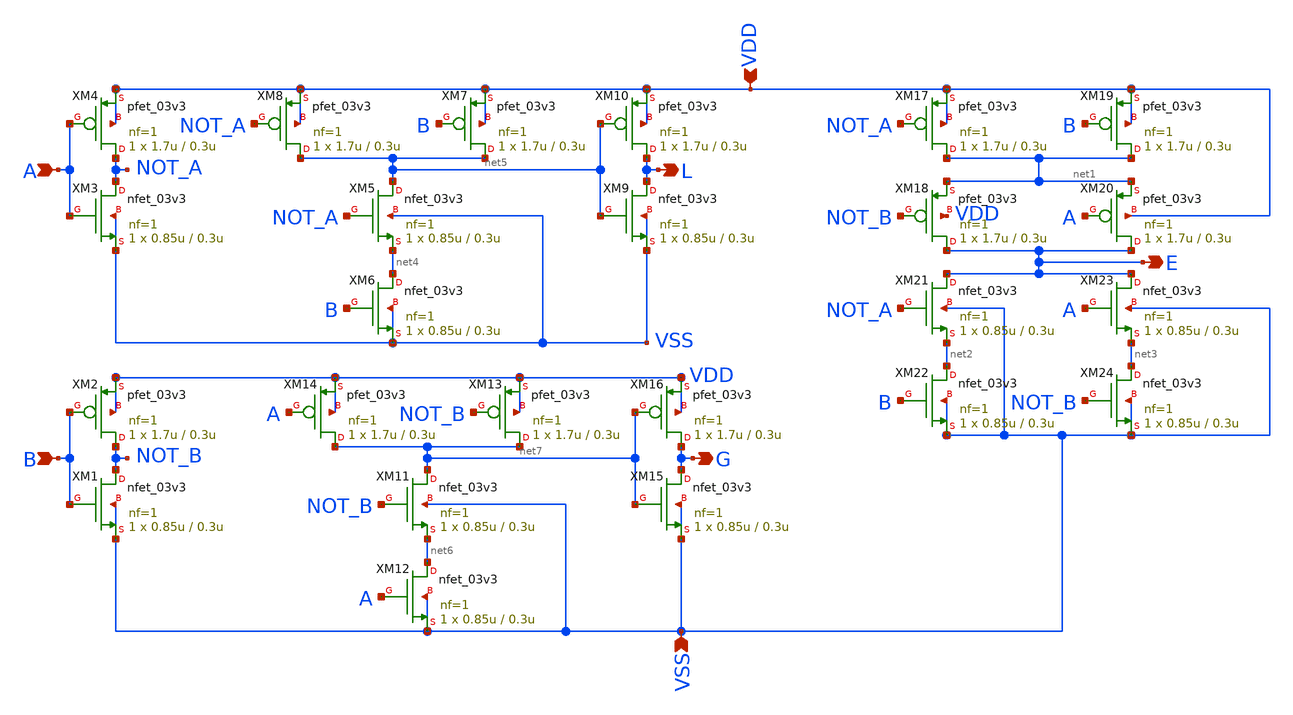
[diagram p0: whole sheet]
** sch_path: cells/comp2/layout/tests/sept5_layout/gf180mcu_gp9t3v3__comp2_1.sch
**.subckt gf180mcu_gp9t3v3__comp2_1 L G E A B VDD VSS
*.opin L
*.opin G
*.opin E
*.ipin A
*.ipin B
*.ipin VDD
*.ipin VSS
XM17 net1 NOT_A VDD VDD pfet_03v3 L=0.3u W=1.7u nf=1 ad='int((nf+1)/2) * W/nf * 0.18u' as='int((nf+2)/2) * W/nf * 0.18u'
+ pd='2*int((nf+1)/2) * (W/nf + 0.18u)' ps='2*int((nf+2)/2) * (W/nf + 0.18u)' nrd='0.18u / W' nrs='0.18u / W'
+ sa=0 sb=0 sd=0 m=1
XM18 E NOT_B net1 VDD pfet_03v3 L=0.3u W=1.7u nf=1 ad='int((nf+1)/2) * W/nf * 0.18u' as='int((nf+2)/2) * W/nf * 0.18u'
+ pd='2*int((nf+1)/2) * (W/nf + 0.18u)' ps='2*int((nf+2)/2) * (W/nf + 0.18u)' nrd='0.18u / W' nrs='0.18u / W'
+ sa=0 sb=0 sd=0 m=1
XM19 net1 B VDD VDD pfet_03v3 L=0.3u W=1.7u nf=1 ad='int((nf+1)/2) * W/nf * 0.18u' as='int((nf+2)/2) * W/nf * 0.18u'
+ pd='2*int((nf+1)/2) * (W/nf + 0.18u)' ps='2*int((nf+2)/2) * (W/nf + 0.18u)' nrd='0.18u / W' nrs='0.18u / W'
+ sa=0 sb=0 sd=0 m=1
XM20 E A net1 VDD pfet_03v3 L=0.3u W=1.7u nf=1 ad='int((nf+1)/2) * W/nf * 0.18u' as='int((nf+2)/2) * W/nf * 0.18u'
+ pd='2*int((nf+1)/2) * (W/nf + 0.18u)' ps='2*int((nf+2)/2) * (W/nf + 0.18u)' nrd='0.18u / W' nrs='0.18u / W'
+ sa=0 sb=0 sd=0 m=1
XM21 E NOT_A net2 VSS nfet_03v3 L=0.3u W=0.85u nf=1 ad='int((nf+1)/2) * W/nf * 0.18u' as='int((nf+2)/2) * W/nf * 0.18u'
+ pd='2*int((nf+1)/2) * (W/nf + 0.18u)' ps='2*int((nf+2)/2) * (W/nf + 0.18u)' nrd='0.18u / W' nrs='0.18u / W'
+ sa=0 sb=0 sd=0 m=1
XM22 net2 B VSS VSS nfet_03v3 L=0.3u W=0.85u nf=1 ad='int((nf+1)/2) * W/nf * 0.18u' as='int((nf+2)/2) * W/nf * 0.18u'
+ pd='2*int((nf+1)/2) * (W/nf + 0.18u)' ps='2*int((nf+2)/2) * (W/nf + 0.18u)' nrd='0.18u / W' nrs='0.18u / W'
+ sa=0 sb=0 sd=0 m=1
XM23 E A net3 VSS nfet_03v3 L=0.3u W=0.85u nf=1 ad='int((nf+1)/2) * W/nf * 0.18u' as='int((nf+2)/2) * W/nf * 0.18u'
+ pd='2*int((nf+1)/2) * (W/nf + 0.18u)' ps='2*int((nf+2)/2) * (W/nf + 0.18u)' nrd='0.18u / W' nrs='0.18u / W'
+ sa=0 sb=0 sd=0 m=1
XM24 net3 NOT_B VSS VSS nfet_03v3 L=0.3u W=0.85u nf=1 ad='int((nf+1)/2) * W/nf * 0.18u' as='int((nf+2)/2) * W/nf * 0.18u'
+ pd='2*int((nf+1)/2) * (W/nf + 0.18u)' ps='2*int((nf+2)/2) * (W/nf + 0.18u)' nrd='0.18u / W' nrs='0.18u / W'
+ sa=0 sb=0 sd=0 m=1
XM1 NOT_B B VSS VSS nfet_03v3 L=0.3u W=0.85u nf=1 ad='int((nf+1)/2) * W/nf * 0.18u' as='int((nf+2)/2) * W/nf * 0.18u'
+ pd='2*int((nf+1)/2) * (W/nf + 0.18u)' ps='2*int((nf+2)/2) * (W/nf + 0.18u)' nrd='0.18u / W' nrs='0.18u / W'
+ sa=0 sb=0 sd=0 m=1
XM2 NOT_B B VDD VDD pfet_03v3 L=0.3u W=1.7u nf=1 ad='int((nf+1)/2) * W/nf * 0.18u' as='int((nf+2)/2) * W/nf * 0.18u'
+ pd='2*int((nf+1)/2) * (W/nf + 0.18u)' ps='2*int((nf+2)/2) * (W/nf + 0.18u)' nrd='0.18u / W' nrs='0.18u / W'
+ sa=0 sb=0 sd=0 m=1
XM3 NOT_A A VSS VSS nfet_03v3 L=0.3u W=0.85u nf=1 ad='int((nf+1)/2) * W/nf * 0.18u' as='int((nf+2)/2) * W/nf * 0.18u'
+ pd='2*int((nf+1)/2) * (W/nf + 0.18u)' ps='2*int((nf+2)/2) * (W/nf + 0.18u)' nrd='0.18u / W' nrs='0.18u / W'
+ sa=0 sb=0 sd=0 m=1
XM4 NOT_A A VDD VDD pfet_03v3 L=0.3u W=1.7u nf=1 ad='int((nf+1)/2) * W/nf * 0.18u' as='int((nf+2)/2) * W/nf * 0.18u'
+ pd='2*int((nf+1)/2) * (W/nf + 0.18u)' ps='2*int((nf+2)/2) * (W/nf + 0.18u)' nrd='0.18u / W' nrs='0.18u / W'
+ sa=0 sb=0 sd=0 m=1
XM5 net5 NOT_A net4 VSS nfet_03v3 L=0.3u W=0.85u nf=1 ad='int((nf+1)/2) * W/nf * 0.18u' as='int((nf+2)/2) * W/nf * 0.18u'
+ pd='2*int((nf+1)/2) * (W/nf + 0.18u)' ps='2*int((nf+2)/2) * (W/nf + 0.18u)' nrd='0.18u / W' nrs='0.18u / W'
+ sa=0 sb=0 sd=0 m=1
XM6 net4 B VSS VSS nfet_03v3 L=0.3u W=0.85u nf=1 ad='int((nf+1)/2) * W/nf * 0.18u' as='int((nf+2)/2) * W/nf * 0.18u'
+ pd='2*int((nf+1)/2) * (W/nf + 0.18u)' ps='2*int((nf+2)/2) * (W/nf + 0.18u)' nrd='0.18u / W' nrs='0.18u / W'
+ sa=0 sb=0 sd=0 m=1
XM7 net5 B VDD VDD pfet_03v3 L=0.3u W=1.7u nf=1 ad='int((nf+1)/2) * W/nf * 0.18u' as='int((nf+2)/2) * W/nf * 0.18u'
+ pd='2*int((nf+1)/2) * (W/nf + 0.18u)' ps='2*int((nf+2)/2) * (W/nf + 0.18u)' nrd='0.18u / W' nrs='0.18u / W'
+ sa=0 sb=0 sd=0 m=1
XM8 net5 NOT_A VDD VDD pfet_03v3 L=0.3u W=1.7u nf=1 ad='int((nf+1)/2) * W/nf * 0.18u' as='int((nf+2)/2) * W/nf * 0.18u'
+ pd='2*int((nf+1)/2) * (W/nf + 0.18u)' ps='2*int((nf+2)/2) * (W/nf + 0.18u)' nrd='0.18u / W' nrs='0.18u / W'
+ sa=0 sb=0 sd=0 m=1
XM9 L net5 VSS VSS nfet_03v3 L=0.3u W=0.85u nf=1 ad='int((nf+1)/2) * W/nf * 0.18u' as='int((nf+2)/2) * W/nf * 0.18u'
+ pd='2*int((nf+1)/2) * (W/nf + 0.18u)' ps='2*int((nf+2)/2) * (W/nf + 0.18u)' nrd='0.18u / W' nrs='0.18u / W'
+ sa=0 sb=0 sd=0 m=1
XM10 L net5 VDD VDD pfet_03v3 L=0.3u W=1.7u nf=1 ad='int((nf+1)/2) * W/nf * 0.18u' as='int((nf+2)/2) * W/nf * 0.18u'
+ pd='2*int((nf+1)/2) * (W/nf + 0.18u)' ps='2*int((nf+2)/2) * (W/nf + 0.18u)' nrd='0.18u / W' nrs='0.18u / W'
+ sa=0 sb=0 sd=0 m=1
XM11 net7 NOT_B net6 VSS nfet_03v3 L=0.3u W=0.85u nf=1 ad='int((nf+1)/2) * W/nf * 0.18u' as='int((nf+2)/2) * W/nf * 0.18u'
+ pd='2*int((nf+1)/2) * (W/nf + 0.18u)' ps='2*int((nf+2)/2) * (W/nf + 0.18u)' nrd='0.18u / W' nrs='0.18u / W'
+ sa=0 sb=0 sd=0 m=1
XM12 net6 A VSS VSS nfet_03v3 L=0.3u W=0.85u nf=1 ad='int((nf+1)/2) * W/nf * 0.18u' as='int((nf+2)/2) * W/nf * 0.18u'
+ pd='2*int((nf+1)/2) * (W/nf + 0.18u)' ps='2*int((nf+2)/2) * (W/nf + 0.18u)' nrd='0.18u / W' nrs='0.18u / W'
+ sa=0 sb=0 sd=0 m=1
XM13 net7 NOT_B VDD VDD pfet_03v3 L=0.3u W=1.7u nf=1 ad='int((nf+1)/2) * W/nf * 0.18u' as='int((nf+2)/2) * W/nf * 0.18u'
+ pd='2*int((nf+1)/2) * (W/nf + 0.18u)' ps='2*int((nf+2)/2) * (W/nf + 0.18u)' nrd='0.18u / W' nrs='0.18u / W'
+ sa=0 sb=0 sd=0 m=1
XM14 net7 A VDD VDD pfet_03v3 L=0.3u W=1.7u nf=1 ad='int((nf+1)/2) * W/nf * 0.18u' as='int((nf+2)/2) * W/nf * 0.18u'
+ pd='2*int((nf+1)/2) * (W/nf + 0.18u)' ps='2*int((nf+2)/2) * (W/nf + 0.18u)' nrd='0.18u / W' nrs='0.18u / W'
+ sa=0 sb=0 sd=0 m=1
XM15 G net7 VSS VSS nfet_03v3 L=0.3u W=0.85u nf=1 ad='int((nf+1)/2) * W/nf * 0.18u' as='int((nf+2)/2) * W/nf * 0.18u'
+ pd='2*int((nf+1)/2) * (W/nf + 0.18u)' ps='2*int((nf+2)/2) * (W/nf + 0.18u)' nrd='0.18u / W' nrs='0.18u / W'
+ sa=0 sb=0 sd=0 m=1
XM16 G net7 VDD VDD pfet_03v3 L=0.3u W=1.7u nf=1 ad='int((nf+1)/2) * W/nf * 0.18u' as='int((nf+2)/2) * W/nf * 0.18u'
+ pd='2*int((nf+1)/2) * (W/nf + 0.18u)' ps='2*int((nf+2)/2) * (W/nf + 0.18u)' nrd='0.18u / W' nrs='0.18u / W'
+ sa=0 sb=0 sd=0 m=1
**.ends
.end
